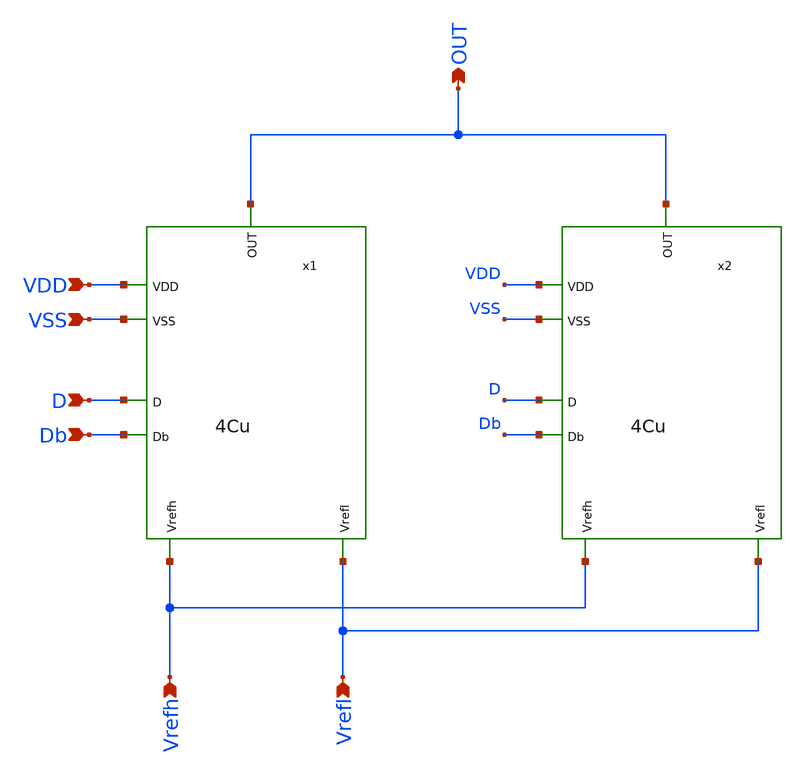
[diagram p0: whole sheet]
** sch_path: 8Cu.sch
**.subckt 8Cu OUT VDD D VSS Vrefh Vrefl Db
*.opin OUT
*.ipin VDD
*.ipin D
*.ipin VSS
*.ipin Vrefh
*.ipin Vrefl
*.ipin Db
x1 OUT VSS VDD Db D Vrefl Vrefh 4Cu
x2 OUT VSS VDD Db D Vrefl Vrefh 4Cu
**.ends
.end
